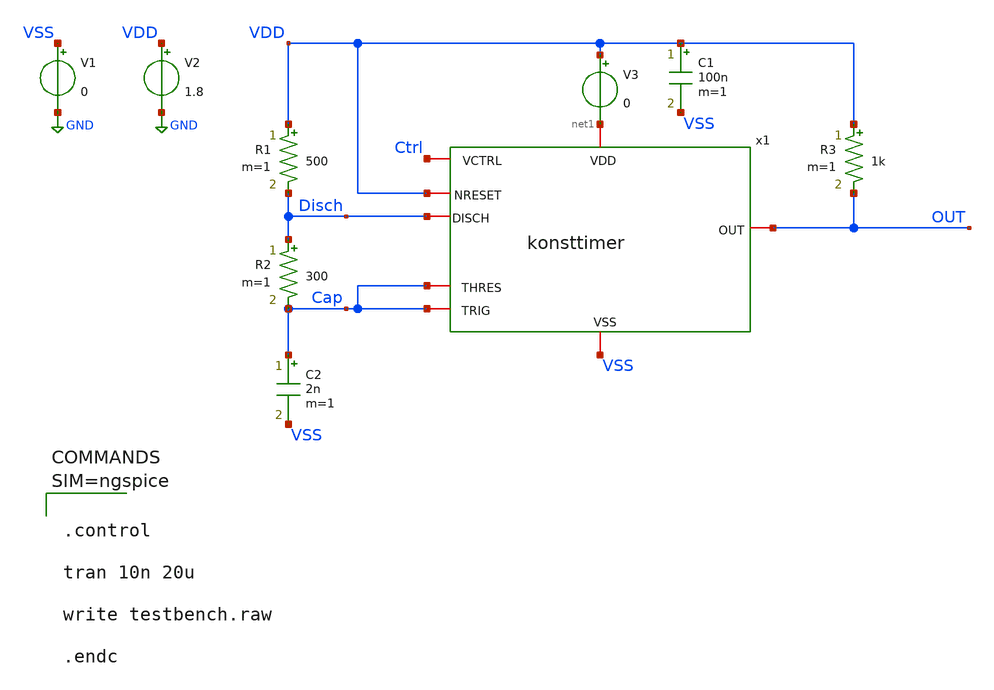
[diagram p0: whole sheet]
** sch_path: xschem/testbench.sch
**.subckt testbench
x1 net1 VDD Cap OUT Ctrl Cap Disch VSS konsttimer
V1 VSS GND 0
V2 VDD GND 1.8
C1 VDD VSS 100n m=1
R1 VDD Disch 500 m=1
R2 Disch Cap 300 m=1
C2 Cap VSS 2n m=1
R3 VDD OUT 1k m=1
V3 VDD net1 0
**** begin user architecture code

** opencircuitdesign pdks install
.lib $::SKYWATER_MODELS/sky130.lib.spice tt





.control

tran 10n 20u

write testbench.raw

.endc



**** end user architecture code
**.ends

* expanding   symbol:  konsttimer.sym # of pins=8
** sym_path: xschem/konsttimer.sym
** sch_path: xschem/konsttimer.sch
.subckt konsttimer VDD NRESET THRES OUT VCTRL TRIG DISCH VSS
*.iopin VDD
*.iopin VSS
*.iopin DISCH
*.iopin VCTRL
*.iopin THRES
*.iopin TRIG
*.iopin NRESET
*.iopin OUT
XM2 net4 net4 VSS VSS sky130_fd_pr__nfet_01v8 L=2 W=20 nf=1 ad='int((1 + 1)/2) * 20 / 1 * 0.29' as='int((1 + 2)/2) * 20 / 1 * 0.29'
+ pd='2*int((1 + 1)/2) * (20 / 1 + 0.29)' ps='2*int((1 + 2)/2) * (20 / 1 + 0.29)' nrd='0.29 / 20 ' nrs='0.29 / 20 '
+ sa=0 sb=0 sd=0 mult=1 m=1
XM1 net1 net4 VSS VSS sky130_fd_pr__nfet_01v8 L=2 W=20 nf=1 ad='int((1 + 1)/2) * 20 / 1 * 0.29' as='int((1 + 2)/2) * 20 / 1 * 0.29'
+ pd='2*int((1 + 1)/2) * (20 / 1 + 0.29)' ps='2*int((1 + 2)/2) * (20 / 1 + 0.29)' nrd='0.29 / 20 ' nrs='0.29 / 20 '
+ sa=0 sb=0 sd=0 mult=1 m=1
XM3 net2 THRES net1 VSS sky130_fd_pr__nfet_01v8 L=2 W=20 nf=1 ad='int((1 + 1)/2) * 20 / 1 * 0.29' as='int((1 + 2)/2) * 20 / 1 * 0.29'
+ pd='2*int((1 + 1)/2) * (20 / 1 + 0.29)' ps='2*int((1 + 2)/2) * (20 / 1 + 0.29)' nrd='0.29 / 20 ' nrs='0.29 / 20 '
+ sa=0 sb=0 sd=0 mult=1 m=1
XM4 net3 VCTRL net1 VSS sky130_fd_pr__nfet_01v8 L=2 W=20 nf=1 ad='int((1 + 1)/2) * 20 / 1 * 0.29' as='int((1 + 2)/2) * 20 / 1 * 0.29'
+ pd='2*int((1 + 1)/2) * (20 / 1 + 0.29)' ps='2*int((1 + 2)/2) * (20 / 1 + 0.29)' nrd='0.29 / 20 ' nrs='0.29 / 20 '
+ sa=0 sb=0 sd=0 mult=1 m=1
XM5 net2 net3 VDD VDD sky130_fd_pr__pfet_01v8 L=2 W=20 nf=1 ad='int((nf+1)/2) * W/nf * 0.29' as='int((nf+2)/2) * W/nf * 0.29'
+ pd='2*int((nf+1)/2) * (W/nf + 0.29)' ps='2*int((nf+2)/2) * (W/nf + 0.29)' nrd='0.29 / W' nrs='0.29 / W'
+ sa=0 sb=0 sd=0 mult=1 m=1
XM6 net3 net3 VDD VDD sky130_fd_pr__pfet_01v8 L=2 W=20 nf=1 ad='int((nf+1)/2) * W/nf * 0.29' as='int((nf+2)/2) * W/nf * 0.29'
+ pd='2*int((nf+1)/2) * (W/nf + 0.29)' ps='2*int((nf+2)/2) * (W/nf + 0.29)' nrd='0.29 / W' nrs='0.29 / W'
+ sa=0 sb=0 sd=0 mult=1 m=1
XM7 net5 net5 VDD VDD sky130_fd_pr__pfet_01v8 L=2 W=20 nf=1 ad='int((nf+1)/2) * W/nf * 0.29' as='int((nf+2)/2) * W/nf * 0.29'
+ pd='2*int((nf+1)/2) * (W/nf + 0.29)' ps='2*int((nf+2)/2) * (W/nf + 0.29)' nrd='0.29 / W' nrs='0.29 / W'
+ sa=0 sb=0 sd=0 mult=1 m=1
XM8 net7 net7 VSS VSS sky130_fd_pr__nfet_01v8 L=2 W=20 nf=1 ad='int((1 + 1)/2) * 20 / 1 * 0.29' as='int((1 + 2)/2) * 20 / 1 * 0.29'
+ pd='2*int((1 + 1)/2) * (20 / 1 + 0.29)' ps='2*int((1 + 2)/2) * (20 / 1 + 0.29)' nrd='0.29 / 20 ' nrs='0.29 / 20 '
+ sa=0 sb=0 sd=0 mult=1 m=1
XM9 net8 net7 VSS VSS sky130_fd_pr__nfet_01v8 L=2 W=20 nf=1 ad='int((1 + 1)/2) * 20 / 1 * 0.29' as='int((1 + 2)/2) * 20 / 1 * 0.29'
+ pd='2*int((1 + 1)/2) * (20 / 1 + 0.29)' ps='2*int((1 + 2)/2) * (20 / 1 + 0.29)' nrd='0.29 / 20 ' nrs='0.29 / 20 '
+ sa=0 sb=0 sd=0 mult=1 m=1
XM10 net7 net6 net9 net9 sky130_fd_pr__pfet_01v8 L=2 W=20 nf=1 ad='int((nf+1)/2) * W/nf * 0.29' as='int((nf+2)/2) * W/nf * 0.29'
+ pd='2*int((nf+1)/2) * (W/nf + 0.29)' ps='2*int((nf+2)/2) * (W/nf + 0.29)' nrd='0.29 / W' nrs='0.29 / W'
+ sa=0 sb=0 sd=0 mult=1 m=1
XM11 net8 TRIG net9 net9 sky130_fd_pr__pfet_01v8 L=2 W=20 nf=1 ad='int((nf+1)/2) * W/nf * 0.29' as='int((nf+2)/2) * W/nf * 0.29'
+ pd='2*int((nf+1)/2) * (W/nf + 0.29)' ps='2*int((nf+2)/2) * (W/nf + 0.29)' nrd='0.29 / W' nrs='0.29 / W'
+ sa=0 sb=0 sd=0 mult=1 m=1
XM12 net9 net5 VDD VDD sky130_fd_pr__pfet_01v8 L=2 W=20 nf=1 ad='int((nf+1)/2) * W/nf * 0.29' as='int((nf+2)/2) * W/nf * 0.29'
+ pd='2*int((nf+1)/2) * (W/nf + 0.29)' ps='2*int((nf+2)/2) * (W/nf + 0.29)' nrd='0.29 / W' nrs='0.29 / W'
+ sa=0 sb=0 sd=0 mult=1 m=1
XM13 net10 net2 VDD VDD sky130_fd_pr__pfet_01v8 L=2 W=20 nf=1 ad='int((nf+1)/2) * W/nf * 0.29' as='int((nf+2)/2) * W/nf * 0.29'
+ pd='2*int((nf+1)/2) * (W/nf + 0.29)' ps='2*int((nf+2)/2) * (W/nf + 0.29)' nrd='0.29 / W' nrs='0.29 / W'
+ sa=0 sb=0 sd=0 mult=1 m=1
XM14 net8 NRESET VDD VDD sky130_fd_pr__pfet_01v8 L=2 W=20 nf=1 ad='int((nf+1)/2) * W/nf * 0.29' as='int((nf+2)/2) * W/nf * 0.29'
+ pd='2*int((nf+1)/2) * (W/nf + 0.29)' ps='2*int((nf+2)/2) * (W/nf + 0.29)' nrd='0.29 / W' nrs='0.29 / W'
+ sa=0 sb=0 sd=0 mult=1 m=1
XM15 net11 net5 VDD VDD sky130_fd_pr__pfet_01v8 L=2 W=20 nf=1 ad='int((nf+1)/2) * W/nf * 0.29' as='int((nf+2)/2) * W/nf * 0.29'
+ pd='2*int((nf+1)/2) * (W/nf + 0.29)' ps='2*int((nf+2)/2) * (W/nf + 0.29)' nrd='0.29 / W' nrs='0.29 / W'
+ sa=0 sb=0 sd=0 mult=1 m=1
XM16 net12 net5 VDD VDD sky130_fd_pr__pfet_01v8 L=2 W=20 nf=1 ad='int((nf+1)/2) * W/nf * 0.29' as='int((nf+2)/2) * W/nf * 0.29'
+ pd='2*int((nf+1)/2) * (W/nf + 0.29)' ps='2*int((nf+2)/2) * (W/nf + 0.29)' nrd='0.29 / W' nrs='0.29 / W'
+ sa=0 sb=0 sd=0 mult=1 m=1
XM17 net10 net4 VSS VSS sky130_fd_pr__nfet_01v8 L=2 W=20 nf=1 ad='int((1 + 1)/2) * 20 / 1 * 0.29' as='int((1 + 2)/2) * 20 / 1 * 0.29'
+ pd='2*int((1 + 1)/2) * (20 / 1 + 0.29)' ps='2*int((1 + 2)/2) * (20 / 1 + 0.29)' nrd='0.29 / 20 ' nrs='0.29 / 20 '
+ sa=0 sb=0 sd=0 mult=1 m=1
XM18 net12 net10 VSS VSS sky130_fd_pr__nfet_01v8 L=2 W=20 nf=1 ad='int((1 + 1)/2) * 20 / 1 * 0.29' as='int((1 + 2)/2) * 20 / 1 * 0.29'
+ pd='2*int((1 + 1)/2) * (20 / 1 + 0.29)' ps='2*int((1 + 2)/2) * (20 / 1 + 0.29)' nrd='0.29 / 20 ' nrs='0.29 / 20 '
+ sa=0 sb=0 sd=0 mult=1 m=1
XM19 net11 net8 VSS VSS sky130_fd_pr__nfet_01v8 L=2 W=20 nf=1 ad='int((1 + 1)/2) * 20 / 1 * 0.29' as='int((1 + 2)/2) * 20 / 1 * 0.29'
+ pd='2*int((1 + 1)/2) * (20 / 1 + 0.29)' ps='2*int((1 + 2)/2) * (20 / 1 + 0.29)' nrd='0.29 / 20 ' nrs='0.29 / 20 '
+ sa=0 sb=0 sd=0 mult=1 m=1
XM20 net11 net12 VSS VSS sky130_fd_pr__nfet_01v8 L=2 W=20 nf=1 ad='int((1 + 1)/2) * 20 / 1 * 0.29' as='int((1 + 2)/2) * 20 / 1 * 0.29'
+ pd='2*int((1 + 1)/2) * (20 / 1 + 0.29)' ps='2*int((1 + 2)/2) * (20 / 1 + 0.29)' nrd='0.29 / 20 ' nrs='0.29 / 20 '
+ sa=0 sb=0 sd=0 mult=1 m=1
XM21 net12 net11 VSS VSS sky130_fd_pr__nfet_01v8 L=2 W=20 nf=1 ad='int((1 + 1)/2) * 20 / 1 * 0.29' as='int((1 + 2)/2) * 20 / 1 * 0.29'
+ pd='2*int((1 + 1)/2) * (20 / 1 + 0.29)' ps='2*int((1 + 2)/2) * (20 / 1 + 0.29)' nrd='0.29 / 20 ' nrs='0.29 / 20 '
+ sa=0 sb=0 sd=0 mult=1 m=1
XM22 net13 net12 VSS VSS sky130_fd_pr__nfet_01v8 L=2 W=20 nf=1 ad='int((1 + 1)/2) * 20 / 1 * 0.29' as='int((1 + 2)/2) * 20 / 1 * 0.29'
+ pd='2*int((1 + 1)/2) * (20 / 1 + 0.29)' ps='2*int((1 + 2)/2) * (20 / 1 + 0.29)' nrd='0.29 / 20 ' nrs='0.29 / 20 '
+ sa=0 sb=0 sd=0 mult=1 m=1
XM23 net13 net12 VDD VDD sky130_fd_pr__pfet_01v8 L=2 W=20 nf=1 ad='int((nf+1)/2) * W/nf * 0.29' as='int((nf+2)/2) * W/nf * 0.29'
+ pd='2*int((nf+1)/2) * (W/nf + 0.29)' ps='2*int((nf+2)/2) * (W/nf + 0.29)' nrd='0.29 / W' nrs='0.29 / W'
+ sa=0 sb=0 sd=0 mult=1 m=1
XM24 OUT net13 VSS VSS sky130_fd_pr__nfet_01v8 L=2 W=20 nf=1 ad='int((1 + 1)/2) * 20 / 1 * 0.29' as='int((1 + 2)/2) * 20 / 1 * 0.29'
+ pd='2*int((1 + 1)/2) * (20 / 1 + 0.29)' ps='2*int((1 + 2)/2) * (20 / 1 + 0.29)' nrd='0.29 / 20 ' nrs='0.29 / 20 '
+ sa=0 sb=0 sd=0 mult=1 m=1
XM25 OUT net13 VDD VDD sky130_fd_pr__pfet_01v8 L=2 W=20 nf=1 ad='int((nf+1)/2) * W/nf * 0.29' as='int((nf+2)/2) * W/nf * 0.29'
+ pd='2*int((nf+1)/2) * (W/nf + 0.29)' ps='2*int((nf+2)/2) * (W/nf + 0.29)' nrd='0.29 / W' nrs='0.29 / W'
+ sa=0 sb=0 sd=0 mult=1 m=1
XM26 DISCH net13 VSS VSS sky130_fd_pr__nfet_01v8 L=2 W=20 nf=1 ad='int((1 + 1)/2) * 20 / 1 * 0.29' as='int((1 + 2)/2) * 20 / 1 * 0.29'
+ pd='2*int((1 + 1)/2) * (20 / 1 + 0.29)' ps='2*int((1 + 2)/2) * (20 / 1 + 0.29)' nrd='0.29 / 20 ' nrs='0.29 / 20 '
+ sa=0 sb=0 sd=0 mult=10 m=10
XR14 net4 net5 VSS sky130_fd_pr__res_high_po_2p85 L=2.85 mult=1 m=1
XR2 net6 VCTRL VSS sky130_fd_pr__res_high_po_2p85 L=2.85 mult=1 m=1
XR1 VCTRL VDD VSS sky130_fd_pr__res_high_po_2p85 L=2.85 mult=1 m=1
XR3 VSS net6 VSS sky130_fd_pr__res_high_po_2p85 L=2.85 mult=1 m=1
.ends

.GLOBAL GND
.end
